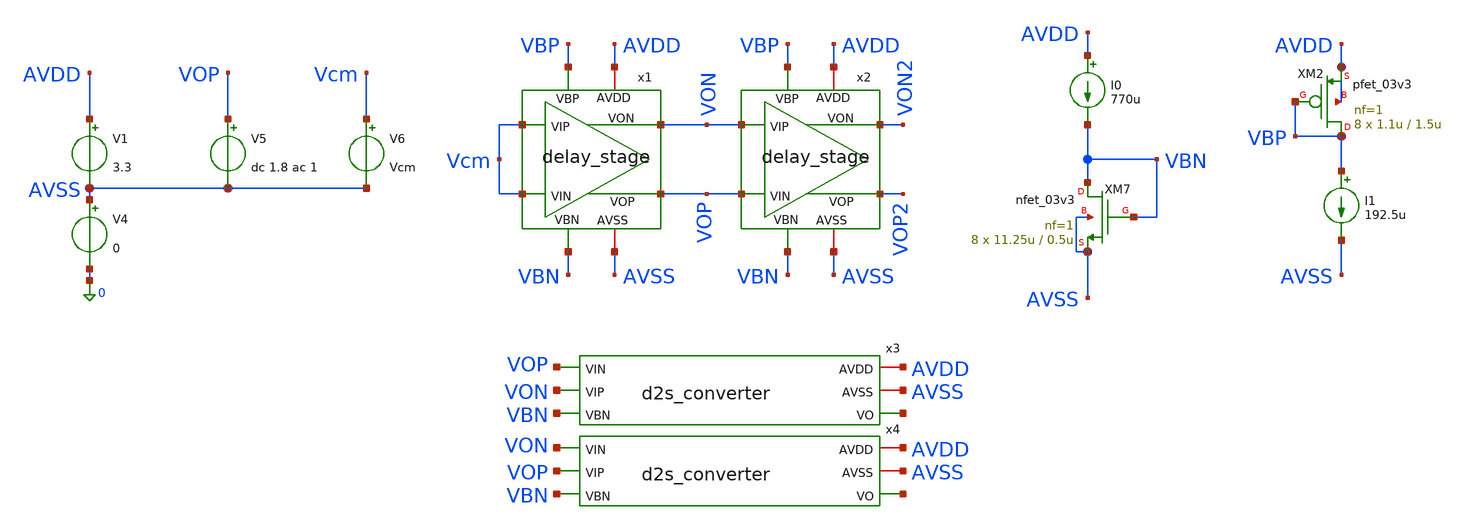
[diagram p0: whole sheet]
** sch_path: designs/libs/tb_analog/tb_delay_stage/tb_delay_stage_ac.sch
**.subckt tb_delay_stage_ac
x1 VOP AVDD Vcm Vcm VON AVSS VBP VBN delay_stage
V1 AVDD AVSS 3.3
V4 AVSS 0 0
V5 VOP AVSS dc 1.8 ac 1
V6 Vcm AVSS Vcm
x2 VOP2 AVDD VON VOP VON2 AVSS VBP VBN delay_stage
XM7 VBN VBN AVSS AVSS nfet_03v3 L=0.5u W=11.25u nf=1 ad='int((nf+1)/2) * W/nf * 0.18u' as='int((nf+2)/2) * W/nf * 0.18u'
+ pd='2*int((nf+1)/2) * (W/nf + 0.18u)' ps='2*int((nf+2)/2) * (W/nf + 0.18u)' nrd='0.18u / W' nrs='0.18u / W'
+ sa=0 sb=0 sd=0 m=8
I0 AVDD VBN 770u
XM2 VBP VBP AVDD AVDD pfet_03v3 L=1.5u W=1.1u nf=1 ad='int((nf+1)/2) * W/nf * 0.18u' as='int((nf+2)/2) * W/nf * 0.18u'
+ pd='2*int((nf+1)/2) * (W/nf + 0.18u)' ps='2*int((nf+2)/2) * (W/nf + 0.18u)' nrd='0.18u / W' nrs='0.18u / W'
+ sa=0 sb=0 sd=0 m=8
I1 VBP AVSS 192.5u
x3 AVDD AVSS VOP VON VBN net1 d2s_converter
x4 AVDD AVSS VON VOP VBN net2 d2s_converter
**** begin user architecture code


.param vbp=2.1 vbn=1.2 Vin=0 Vcm=1.8
* --- AC Impedance Extraction ---
.ac dec 10 1 10G

.control
  run

  * Extract frequency vector
  let freq = frequency

  * Calculate angular frequency (omega)
  let omega = 2 * pi * freq

  * Calculate complex impedance Z = V / I
  * Note: v(VOP) is 1 (AC source), I is current through the AC source (e.g., v1)
  let Z = v(VOP) / -i(v5)

  * Extract imaginary part of admittance (Y = 1/Z)
  * Y_imag = omega * C
  let Y_imag = imag(1/Z)

  * Calculate effective capacitance
  let C_eff = Y_imag / omega

  * Plot capacitance over frequency to verify stability
  plot C_eff ylimit 0 150f

  * Print value at target operating frequency (e.g., 350 MHz)
  meas ac C_target FIND C_eff AT=400e6

write tb_delay_stage_ac.raw
.endc



.include $::180MCU_MODELS/design.ngspice
.lib $::180MCU_MODELS/sm141064.ngspice typical

**** end user architecture code
**.ends

* expanding   symbol:  libs/core_analog/delay_stage/delay_stage.sym # of pins=8
** sym_path: designs/libs/core_analog/delay_stage/delay_stage.sym
** sch_path: designs/libs/core_analog/delay_stage/delay_stage.sch
.subckt delay_stage VOP AVDD VIP VIN VON AVSS VBP VBN
*.ipin VIP
*.ipin VIN
*.opin VOP
*.opin VON
*.iopin AVDD
*.iopin AVSS
*.ipin VBP
*.ipin VBN
XM5 VON VIP net1 AVSS nfet_03v3 L=0.5u W=2.08u nf=1 ad='int((nf+1)/2) * W/nf * 0.18u' as='int((nf+2)/2) * W/nf * 0.18u'
+ pd='2*int((nf+1)/2) * (W/nf + 0.18u)' ps='2*int((nf+2)/2) * (W/nf + 0.18u)' nrd='0.18u / W' nrs='0.18u / W'
+ sa=0 sb=0 sd=0 m=8
XM2 VON VON AVDD AVDD pfet_03v3 L=1.5u W=1.1u nf=1 ad='int((nf+1)/2) * W/nf * 0.18u' as='int((nf+2)/2) * W/nf * 0.18u'
+ pd='2*int((nf+1)/2) * (W/nf + 0.18u)' ps='2*int((nf+2)/2) * (W/nf + 0.18u)' nrd='0.18u / W' nrs='0.18u / W'
+ sa=0 sb=0 sd=0 m=8
XM6 VOP VIN net1 AVSS nfet_03v3 L=0.5u W=2.08u nf=1 ad='int((nf+1)/2) * W/nf * 0.18u' as='int((nf+2)/2) * W/nf * 0.18u'
+ pd='2*int((nf+1)/2) * (W/nf + 0.18u)' ps='2*int((nf+2)/2) * (W/nf + 0.18u)' nrd='0.18u / W' nrs='0.18u / W'
+ sa=0 sb=0 sd=0 m=8
XM1 VON VBP AVDD AVDD pfet_03v3 L=1.5u W=1.1u nf=1 ad='int((nf+1)/2) * W/nf * 0.18u' as='int((nf+2)/2) * W/nf * 0.18u'
+ pd='2*int((nf+1)/2) * (W/nf + 0.18u)' ps='2*int((nf+2)/2) * (W/nf + 0.18u)' nrd='0.18u / W' nrs='0.18u / W'
+ sa=0 sb=0 sd=0 m=8
XM3 VOP VBP AVDD AVDD pfet_03v3 L=1.5u W=1.1u nf=1 ad='int((nf+1)/2) * W/nf * 0.18u' as='int((nf+2)/2) * W/nf * 0.18u'
+ pd='2*int((nf+1)/2) * (W/nf + 0.18u)' ps='2*int((nf+2)/2) * (W/nf + 0.18u)' nrd='0.18u / W' nrs='0.18u / W'
+ sa=0 sb=0 sd=0 m=8
XM4 VOP VOP AVDD AVDD pfet_03v3 L=1.5u W=1.1u nf=1 ad='int((nf+1)/2) * W/nf * 0.18u' as='int((nf+2)/2) * W/nf * 0.18u'
+ pd='2*int((nf+1)/2) * (W/nf + 0.18u)' ps='2*int((nf+2)/2) * (W/nf + 0.18u)' nrd='0.18u / W' nrs='0.18u / W'
+ sa=0 sb=0 sd=0 m=8
XM8 net1 VBN AVSS AVSS nfet_03v3 L=0.5u W=11.25u nf=1 ad='int((nf+1)/2) * W/nf * 0.18u' as='int((nf+2)/2) * W/nf * 0.18u'
+ pd='2*int((nf+1)/2) * (W/nf + 0.18u)' ps='2*int((nf+2)/2) * (W/nf + 0.18u)' nrd='0.18u / W' nrs='0.18u / W'
+ sa=0 sb=0 sd=0 m=8
.ends


* expanding   symbol:  libs/core_analog/d2s_converter/d2s_converter.sym # of pins=6
** sym_path: designs/libs/core_analog/d2s_converter/d2s_converter.sym
** sch_path: designs/libs/core_analog/d2s_converter/d2s_converter.sch
.subckt d2s_converter AVDD AVSS VIN VIP VBN VO
*.iopin AVDD
*.iopin AVSS
*.ipin VIN
*.ipin VIP
*.opin VO
*.ipin VBN
XM2 VOPB VIN i1 AVSS nfet_03v3 L=0.3u W=1.9u nf=1 ad='int((nf+1)/2) * W/nf * 0.18u' as='int((nf+2)/2) * W/nf * 0.18u'
+ pd='2*int((nf+1)/2) * (W/nf + 0.18u)' ps='2*int((nf+2)/2) * (W/nf + 0.18u)' nrd='0.18u / W' nrs='0.18u / W'
+ sa=0 sb=0 sd=0 m=4
XM4 VOPB VOPB AVDD AVDD pfet_03v3 L=0.3u W=1.4u nf=1 ad='int((nf+1)/2) * W/nf * 0.18u' as='int((nf+2)/2) * W/nf * 0.18u'
+ pd='2*int((nf+1)/2) * (W/nf + 0.18u)' ps='2*int((nf+2)/2) * (W/nf + 0.18u)' nrd='0.18u / W' nrs='0.18u / W'
+ sa=0 sb=0 sd=0 m=4
XM11 VOB VOB AVSS AVSS nfet_03v3 L=0.3u W=1.5u nf=1 ad='int((nf+1)/2) * W/nf * 0.18u' as='int((nf+2)/2) * W/nf * 0.18u'
+ pd='2*int((nf+1)/2) * (W/nf + 0.18u)' ps='2*int((nf+2)/2) * (W/nf + 0.18u)' nrd='0.18u / W' nrs='0.18u / W'
+ sa=0 sb=0 sd=0 m=4
XM13 VOB VOP AVDD AVDD pfet_03v3 L=0.3u W=2u nf=1 ad='int((nf+1)/2) * W/nf * 0.18u' as='int((nf+2)/2) * W/nf * 0.18u'
+ pd='2*int((nf+1)/2) * (W/nf + 0.18u)' ps='2*int((nf+2)/2) * (W/nf + 0.18u)' nrd='0.18u / W' nrs='0.18u / W'
+ sa=0 sb=0 sd=0 m=4
XM3 VOP VIP i1 AVSS nfet_03v3 L=0.3u W=1.9u nf=1 ad='int((nf+1)/2) * W/nf * 0.18u' as='int((nf+2)/2) * W/nf * 0.18u'
+ pd='2*int((nf+1)/2) * (W/nf + 0.18u)' ps='2*int((nf+2)/2) * (W/nf + 0.18u)' nrd='0.18u / W' nrs='0.18u / W'
+ sa=0 sb=0 sd=0 m=4
XM5 VOP VOPB AVDD AVDD pfet_03v3 L=0.3u W=1.4u nf=1 ad='int((nf+1)/2) * W/nf * 0.18u' as='int((nf+2)/2) * W/nf * 0.18u'
+ pd='2*int((nf+1)/2) * (W/nf + 0.18u)' ps='2*int((nf+2)/2) * (W/nf + 0.18u)' nrd='0.18u / W' nrs='0.18u / W'
+ sa=0 sb=0 sd=0 m=4
XM7 VONB VIP i2 AVSS nfet_03v3 L=0.3u W=1.9u nf=1 ad='int((nf+1)/2) * W/nf * 0.18u' as='int((nf+2)/2) * W/nf * 0.18u'
+ pd='2*int((nf+1)/2) * (W/nf + 0.18u)' ps='2*int((nf+2)/2) * (W/nf + 0.18u)' nrd='0.18u / W' nrs='0.18u / W'
+ sa=0 sb=0 sd=0 m=4
XM8 VONB VONB AVDD AVDD pfet_03v3 L=0.3u W=1.4u nf=1 ad='int((nf+1)/2) * W/nf * 0.18u' as='int((nf+2)/2) * W/nf * 0.18u'
+ pd='2*int((nf+1)/2) * (W/nf + 0.18u)' ps='2*int((nf+2)/2) * (W/nf + 0.18u)' nrd='0.18u / W' nrs='0.18u / W'
+ sa=0 sb=0 sd=0 m=4
XM9 VON VIN i2 AVSS nfet_03v3 L=0.3u W=1.9u nf=1 ad='int((nf+1)/2) * W/nf * 0.18u' as='int((nf+2)/2) * W/nf * 0.18u'
+ pd='2*int((nf+1)/2) * (W/nf + 0.18u)' ps='2*int((nf+2)/2) * (W/nf + 0.18u)' nrd='0.18u / W' nrs='0.18u / W'
+ sa=0 sb=0 sd=0 m=4
XM10 VON VONB AVDD AVDD pfet_03v3 L=0.3u W=1.4u nf=1 ad='int((nf+1)/2) * W/nf * 0.18u' as='int((nf+2)/2) * W/nf * 0.18u'
+ pd='2*int((nf+1)/2) * (W/nf + 0.18u)' ps='2*int((nf+2)/2) * (W/nf + 0.18u)' nrd='0.18u / W' nrs='0.18u / W'
+ sa=0 sb=0 sd=0 m=4
XM14 VO VON AVDD AVDD pfet_03v3 L=0.3u W=2u nf=1 ad='int((nf+1)/2) * W/nf * 0.18u' as='int((nf+2)/2) * W/nf * 0.18u'
+ pd='2*int((nf+1)/2) * (W/nf + 0.18u)' ps='2*int((nf+2)/2) * (W/nf + 0.18u)' nrd='0.18u / W' nrs='0.18u / W'
+ sa=0 sb=0 sd=0 m=4
XM12 VO VOB AVSS AVSS nfet_03v3 L=0.3u W=1.5u nf=1 ad='int((nf+1)/2) * W/nf * 0.18u' as='int((nf+2)/2) * W/nf * 0.18u'
+ pd='2*int((nf+1)/2) * (W/nf + 0.18u)' ps='2*int((nf+2)/2) * (W/nf + 0.18u)' nrd='0.18u / W' nrs='0.18u / W'
+ sa=0 sb=0 sd=0 m=4
XM1 i1 VBN AVSS AVSS nfet_03v3 L=0.5u W=11.25u nf=1 ad='int((nf+1)/2) * W/nf * 0.18u' as='int((nf+2)/2) * W/nf * 0.18u'
+ pd='2*int((nf+1)/2) * (W/nf + 0.18u)' ps='2*int((nf+2)/2) * (W/nf + 0.18u)' nrd='0.18u / W' nrs='0.18u / W'
+ sa=0 sb=0 sd=0 m=4
XM6 i2 VBN AVSS AVSS nfet_03v3 L=0.5u W=11.25u nf=1 ad='int((nf+1)/2) * W/nf * 0.18u' as='int((nf+2)/2) * W/nf * 0.18u'
+ pd='2*int((nf+1)/2) * (W/nf + 0.18u)' ps='2*int((nf+2)/2) * (W/nf + 0.18u)' nrd='0.18u / W' nrs='0.18u / W'
+ sa=0 sb=0 sd=0 m=4
.ends

.end
